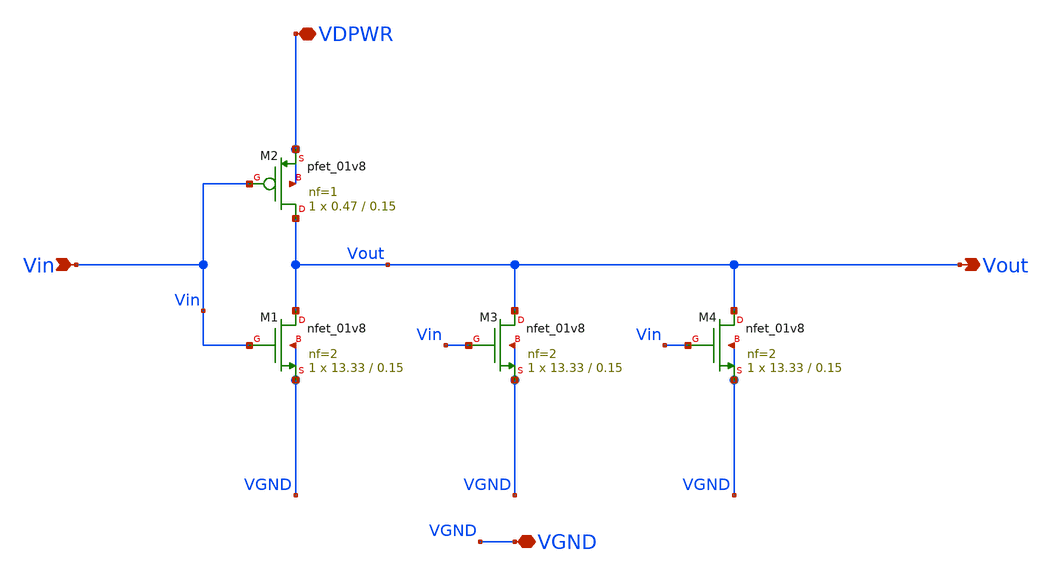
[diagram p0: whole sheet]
** sch_path: tt_um_emmersonv_tiq_adc/xschem/INVERTER_SIZES/inverter_p0o47_n40.sch
**.subckt inverter_p0o47_n40 Vout Vin VDPWR VGND
*.opin Vout
*.ipin Vin
*.iopin VDPWR
*.iopin VGND
XM1 Vout Vin VGND VGND sky130_fd_pr__nfet_01v8 L=0.15 W=13.33 nf=2 ad='int((nf+1)/2) * W/nf * 0.29' as='int((nf+2)/2) * W/nf * 0.29'
+ pd='2*int((nf+1)/2) * (W/nf + 0.29)' ps='2*int((nf+2)/2) * (W/nf + 0.29)' nrd='0.29 / W' nrs='0.29 / W'
+ sa=0 sb=0 sd=0 mult=1 m=1
XM2 Vout Vin VDPWR VDPWR sky130_fd_pr__pfet_01v8 L=0.15 W=0.47 nf=1 ad='int((nf+1)/2) * W/nf * 0.29'
+ as='int((nf+2)/2) * W/nf * 0.29' pd='2*int((nf+1)/2) * (W/nf + 0.29)' ps='2*int((nf+2)/2) * (W/nf + 0.29)'
+ nrd='0.29 / W' nrs='0.29 / W' sa=0 sb=0 sd=0 mult=1 m=1
XM3 Vout Vin VGND VGND sky130_fd_pr__nfet_01v8 L=0.15 W=13.33 nf=2 ad='int((nf+1)/2) * W/nf * 0.29' as='int((nf+2)/2) * W/nf * 0.29'
+ pd='2*int((nf+1)/2) * (W/nf + 0.29)' ps='2*int((nf+2)/2) * (W/nf + 0.29)' nrd='0.29 / W' nrs='0.29 / W'
+ sa=0 sb=0 sd=0 mult=1 m=1
XM4 Vout Vin VGND VGND sky130_fd_pr__nfet_01v8 L=0.15 W=13.33 nf=2 ad='int((nf+1)/2) * W/nf * 0.29' as='int((nf+2)/2) * W/nf * 0.29'
+ pd='2*int((nf+1)/2) * (W/nf + 0.29)' ps='2*int((nf+2)/2) * (W/nf + 0.29)' nrd='0.29 / W' nrs='0.29 / W'
+ sa=0 sb=0 sd=0 mult=1 m=1
**.ends
.end
